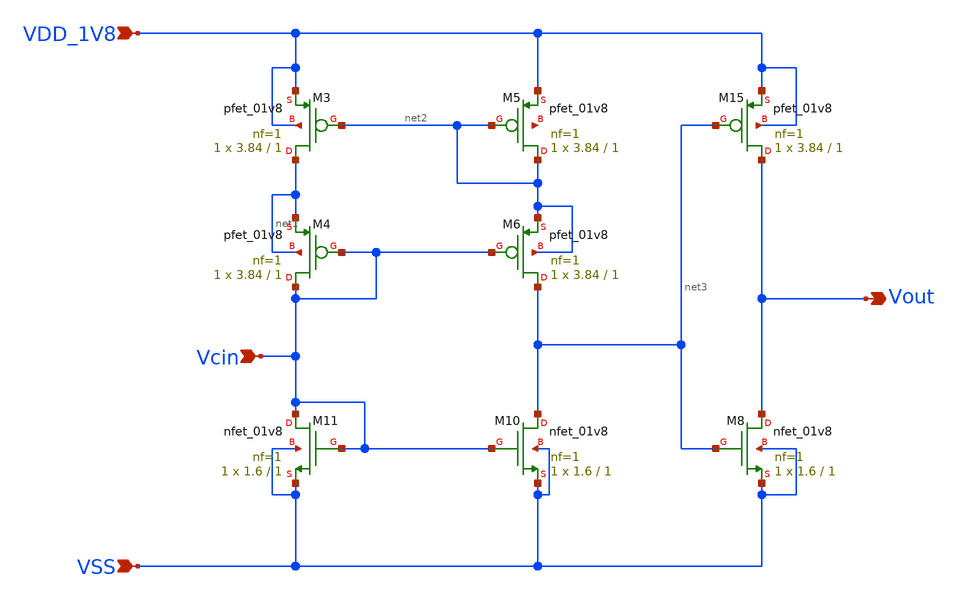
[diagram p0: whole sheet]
** sch_path: design/CNR_GR06_SKY130NM/New_Comp.sch
**.subckt New_Comp VDD_1V8 VSS Vout Vcin
*.ipin VDD_1V8
*.ipin VSS
*.opin Vout
*.ipin Vcin
XM3 net1 net2 VDD_1V8 VDD_1V8 sky130_fd_pr__pfet_01v8 L=1 W=3.84 nf=1 ad='int((nf+1)/2) * W/nf * 0.29'
+ as='int((nf+2)/2) * W/nf * 0.29' pd='2*int((nf+1)/2) * (W/nf + 0.29)' ps='2*int((nf+2)/2) * (W/nf + 0.29)'
+ nrd='0.29 / W' nrs='0.29 / W' sa=0 sb=0 sd=0 mult=1 m=1
XM10 net3 Vcin VSS VSS sky130_fd_pr__nfet_01v8 L=1 W=1.6 nf=1 ad='int((nf+1)/2) * W/nf * 0.29' as='int((nf+2)/2) * W/nf * 0.29'
+ pd='2*int((nf+1)/2) * (W/nf + 0.29)' ps='2*int((nf+2)/2) * (W/nf + 0.29)' nrd='0.29 / W' nrs='0.29 / W'
+ sa=0 sb=0 sd=0 mult=1 m=1
XM11 Vcin Vcin VSS VSS sky130_fd_pr__nfet_01v8 L=1 W=1.6 nf=1 ad='int((nf+1)/2) * W/nf * 0.29' as='int((nf+2)/2) * W/nf * 0.29'
+ pd='2*int((nf+1)/2) * (W/nf + 0.29)' ps='2*int((nf+2)/2) * (W/nf + 0.29)' nrd='0.29 / W' nrs='0.29 / W'
+ sa=0 sb=0 sd=0 mult=1 m=1
XM5 net2 net2 VDD_1V8 net4 sky130_fd_pr__pfet_01v8 L=1 W=3.84 nf=1 ad='int((nf+1)/2) * W/nf * 0.29' as='int((nf+2)/2) * W/nf * 0.29'
+ pd='2*int((nf+1)/2) * (W/nf + 0.29)' ps='2*int((nf+2)/2) * (W/nf + 0.29)' nrd='0.29 / W' nrs='0.29 / W'
+ sa=0 sb=0 sd=0 mult=1 m=1
XM15 Vout net3 VDD_1V8 VDD_1V8 sky130_fd_pr__pfet_01v8 L=1 W=3.84 nf=1 ad='int((nf+1)/2) * W/nf * 0.29'
+ as='int((nf+2)/2) * W/nf * 0.29' pd='2*int((nf+1)/2) * (W/nf + 0.29)' ps='2*int((nf+2)/2) * (W/nf + 0.29)'
+ nrd='0.29 / W' nrs='0.29 / W' sa=0 sb=0 sd=0 mult=1 m=1
XM4 Vcin Vcin net1 net1 sky130_fd_pr__pfet_01v8 L=1 W=3.84 nf=1 ad='int((nf+1)/2) * W/nf * 0.29' as='int((nf+2)/2) * W/nf * 0.29'
+ pd='2*int((nf+1)/2) * (W/nf + 0.29)' ps='2*int((nf+2)/2) * (W/nf + 0.29)' nrd='0.29 / W' nrs='0.29 / W'
+ sa=0 sb=0 sd=0 mult=1 m=1
XM6 net3 Vcin net2 net2 sky130_fd_pr__pfet_01v8 L=1 W=3.84 nf=1 ad='int((nf+1)/2) * W/nf * 0.29' as='int((nf+2)/2) * W/nf * 0.29'
+ pd='2*int((nf+1)/2) * (W/nf + 0.29)' ps='2*int((nf+2)/2) * (W/nf + 0.29)' nrd='0.29 / W' nrs='0.29 / W'
+ sa=0 sb=0 sd=0 mult=1 m=1
XM8 Vout net3 VSS VSS sky130_fd_pr__nfet_01v8 L=1 W=1.6 nf=1 ad='int((nf+1)/2) * W/nf * 0.29' as='int((nf+2)/2) * W/nf * 0.29'
+ pd='2*int((nf+1)/2) * (W/nf + 0.29)' ps='2*int((nf+2)/2) * (W/nf + 0.29)' nrd='0.29 / W' nrs='0.29 / W'
+ sa=0 sb=0 sd=0 mult=1 m=1
**.ends
.end
